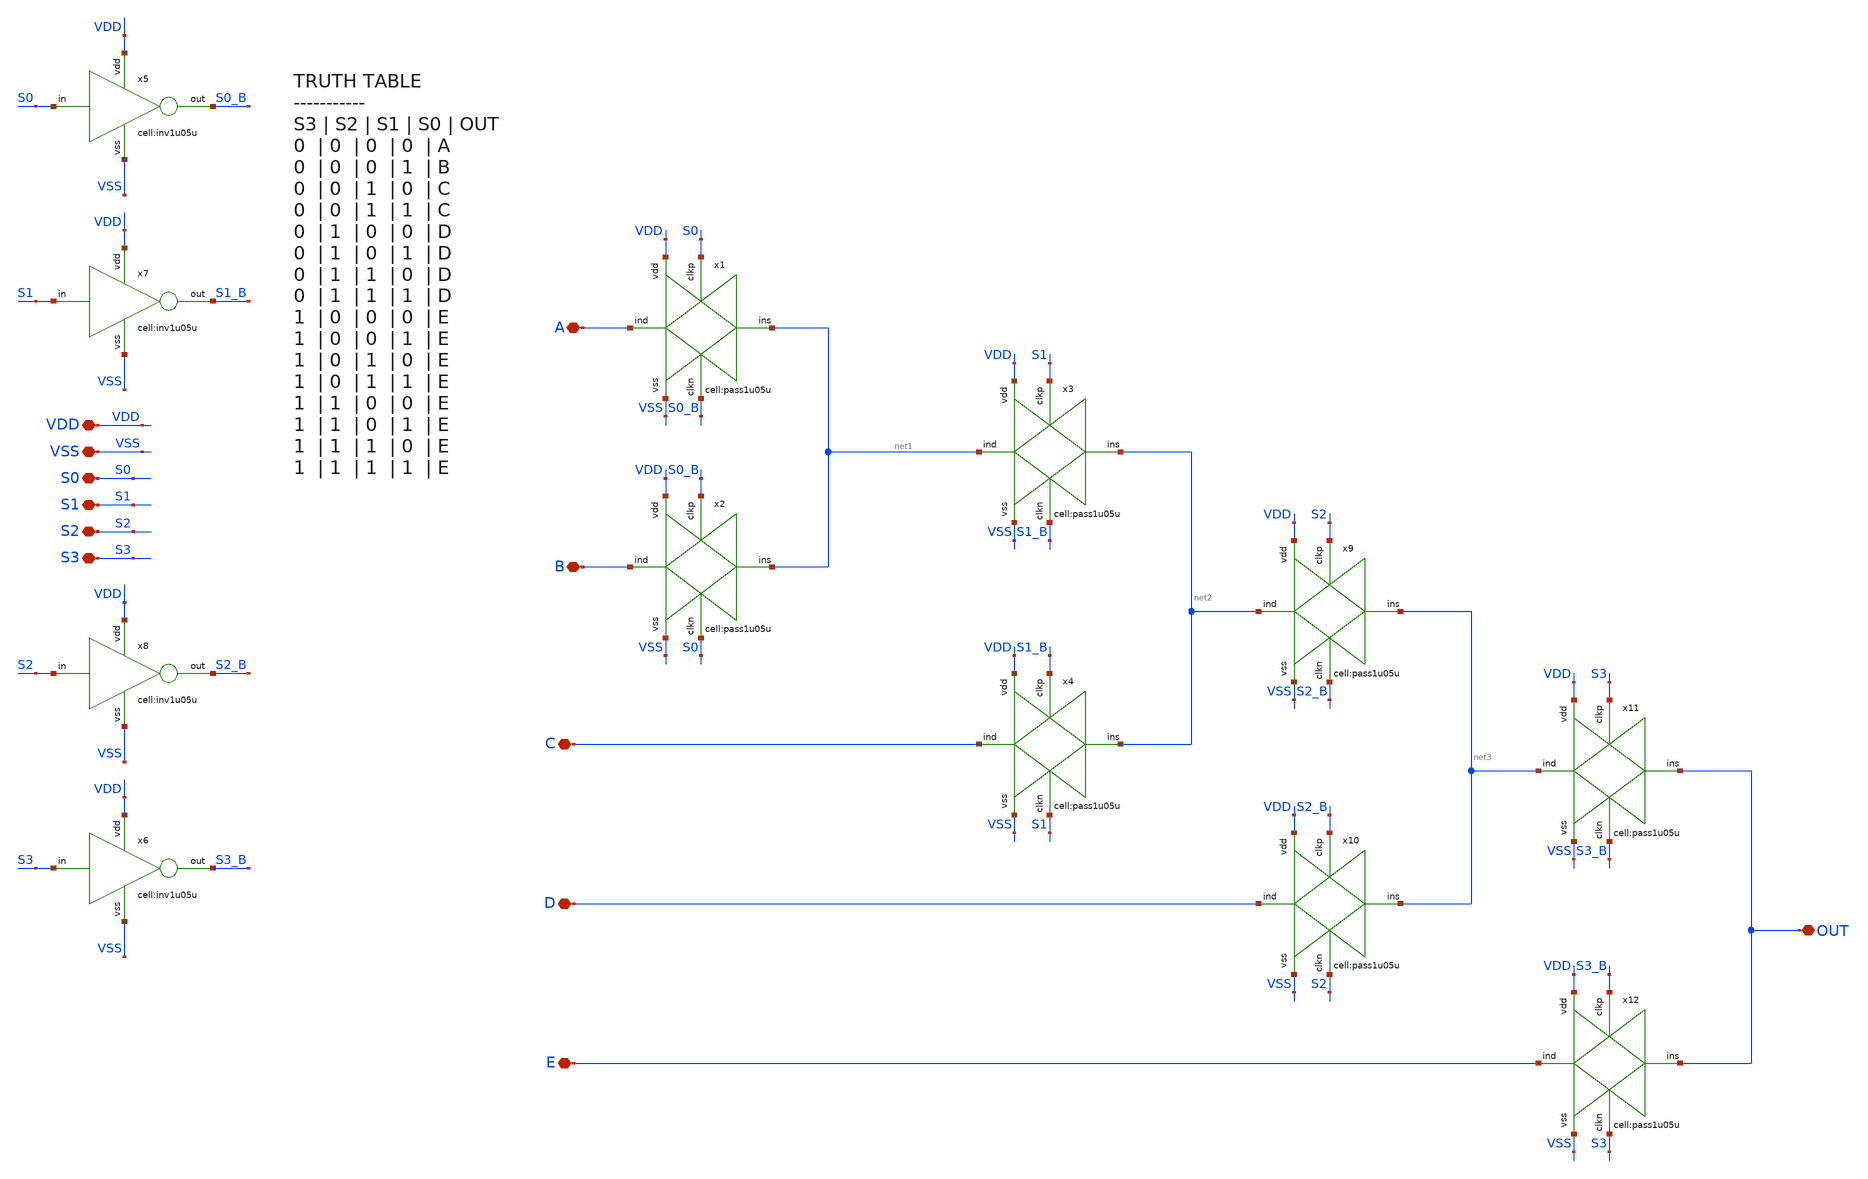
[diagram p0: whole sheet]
** sch_path: designs/libs/core_analog/asc_5_1_MUX/asc_5_1_MUX.sch
**.subckt asc_5_1_MUX A B C OUT VDD VSS S0 S1 S2 S3 D E
*.iopin A
*.iopin B
*.iopin C
*.iopin OUT
*.iopin VDD
*.iopin VSS
*.iopin S0
*.iopin S1
*.iopin S2
*.iopin S3
*.iopin D
*.iopin E
x2 B VSS S0 net1 S0_B VDD pass1u05u
x1 A VSS S0_B net1 S0 VDD pass1u05u
x3 net1 VSS S1_B net2 S1 VDD pass1u05u
x4 C VSS S1 net2 S1_B VDD pass1u05u
x7 S1 VDD S1_B VSS inv1u05u
x5 S0 VDD S0_B VSS inv1u05u
x6 S3 VDD S3_B VSS inv1u05u
x8 S2 VDD S2_B VSS inv1u05u
x9 net2 VSS S2_B net3 S2 VDD pass1u05u
x10 D VSS S2 net3 S2_B VDD pass1u05u
x11 net3 VSS S3_B OUT S3 VDD pass1u05u
x12 E VSS S3 OUT S3_B VDD pass1u05u
**.ends
.end
